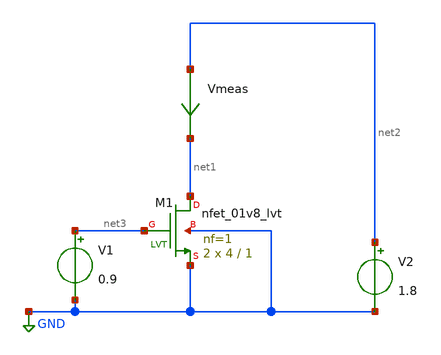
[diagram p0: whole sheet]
** sch_path: xschem/misc/testing/width.sch
**.subckt width
V2 net2 GND 1.8
V1 net3 GND 0.9
Vmeas net2 net1 0
.save i(vmeas)
XM1 net1 net3 GND GND sky130_fd_pr__nfet_01v8_lvt L=1 W=4 nf=1 ad='int((nf+1)/2) * W/nf * 0.29' as='int((nf+2)/2) * W/nf * 0.29'
+ pd='2*int((nf+1)/2) * (W/nf + 0.29)' ps='2*int((nf+2)/2) * (W/nf + 0.29)' nrd='0.29 / W' nrs='0.29 / W'
+ sa=0 sb=0 sd=0 mult=2 m=2
**** begin user architecture code

** opencircuitdesign pdks install
.lib $::SKYWATER_MODELS/sky130.lib.spice tt




.options savecurrents

*** plot temperature coefficient
*Vdd VDD GND 3.3
*V_en en GND 3.3
*.dc temp -40 140 1
.control
save all
run
dc temp -40 100 1
plot Vmeas#branch




.endc



*** plot voltage coefficient
*Vdd VDD GND 3.3
*V_en en GND 3.3
*.dc Vdd 2 4 0.1
*.control
*run
*plot deriv(V(Vbgp))
*.endc

*** plot temperature coefficient
*Vdd VDD GND 3.3
*V_en en GND 3.3
*.dc temp -40 140 1
*.control
*run
*plot deriv(V(Vbgp))/1.202344
*.endc



*** enable pin
*Vdd VDD GND 3.3
*V_en en GND PULSE(0 3.3 0 200us 200us 600us 2000us 0)
*.tran 1u 2000us
*.control
*run
*plot V(en)
*plot -I(VDD)
*.endc


**** end user architecture code
**.ends
.GLOBAL GND
.end
